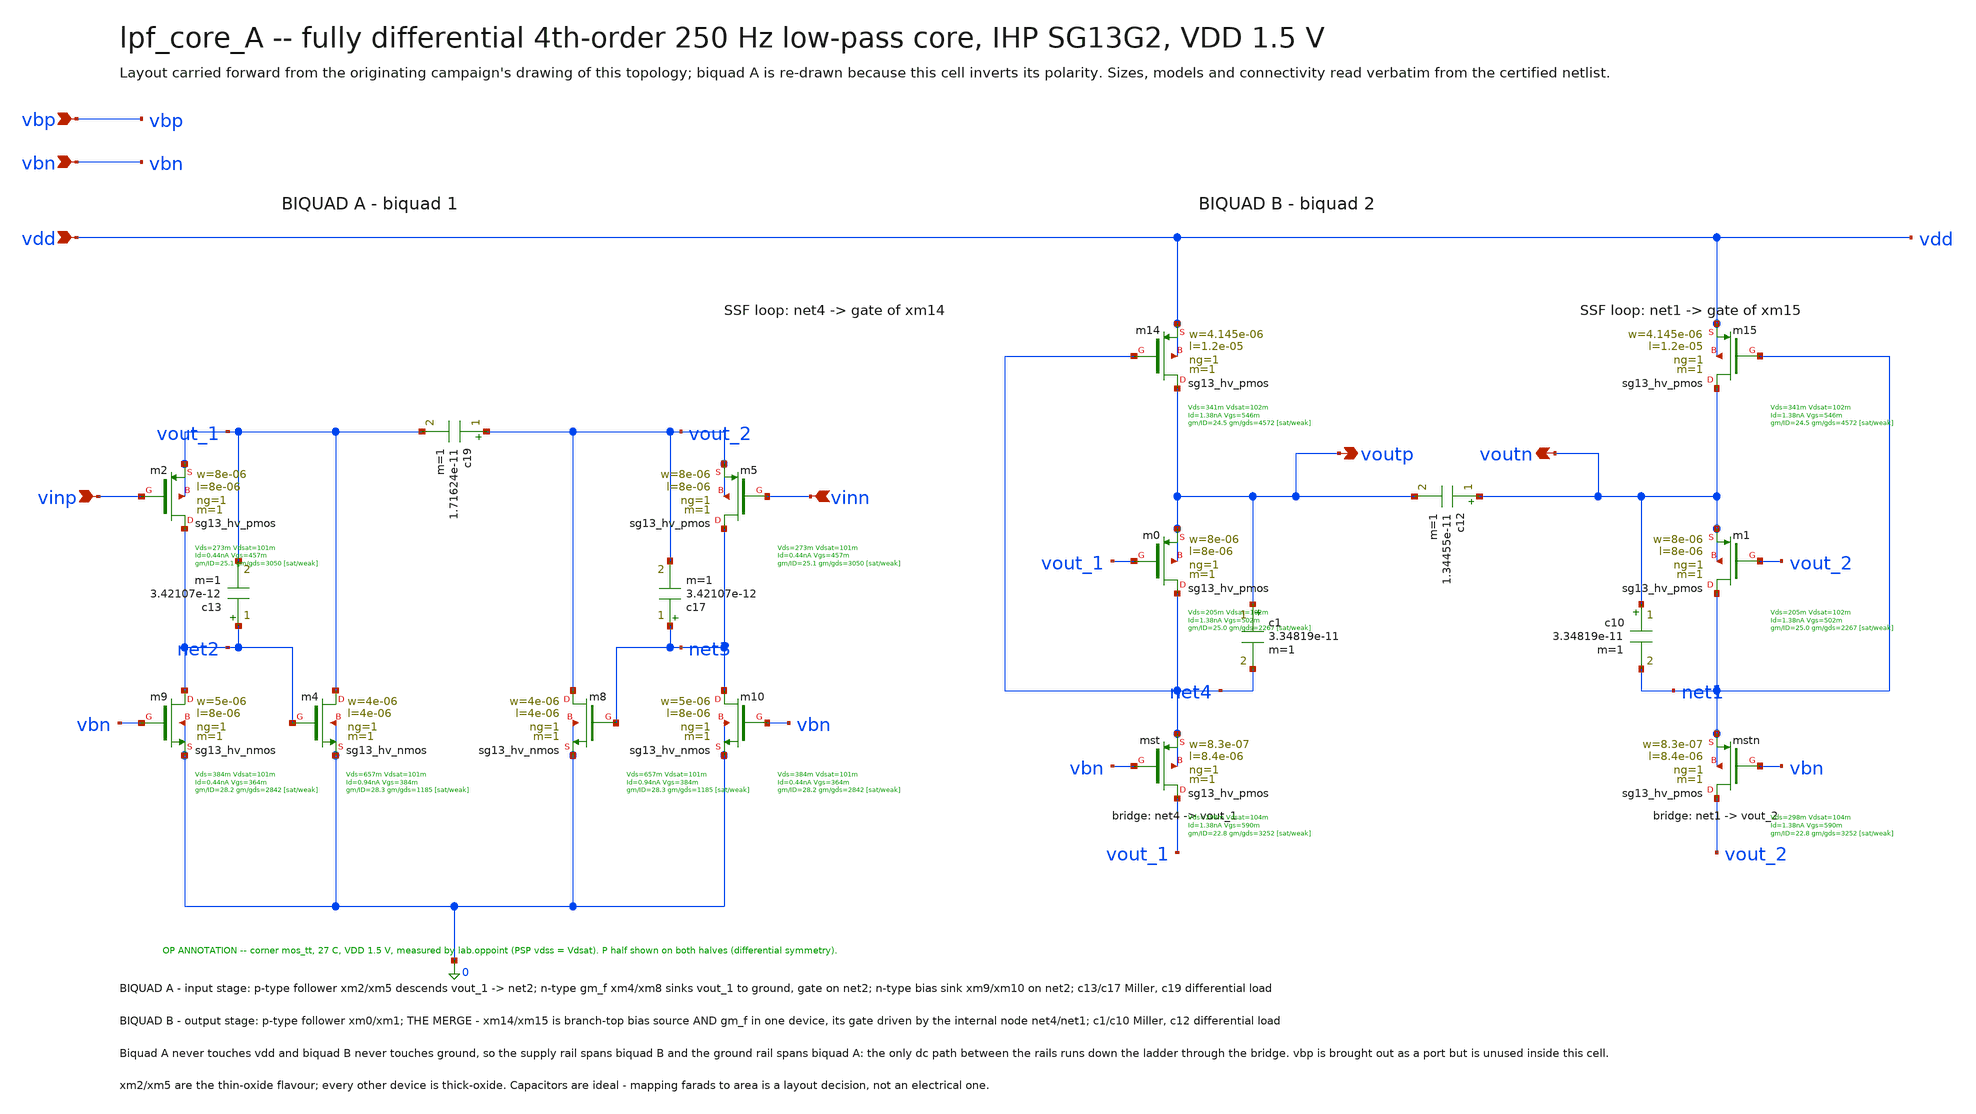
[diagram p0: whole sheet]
** sch_path: signoff/A-minarea/lpf_core_A.sch
**.subckt lpf_core_A vinp vinn voutp voutn vdd vbn vbp
*.ipin vinp
*.ipin vinn
*.opin voutp
*.opin voutn
*.ipin vdd
*.ipin vbn
*.ipin vbp
Xm2 net2 vinp vout_1 vout_1 sg13_hv_pmos w=8e-06 l=8e-06 ng=1 m=1 mm_ok=1
Xm5 net3 vinn vout_2 vout_2 sg13_hv_pmos w=8e-06 l=8e-06 ng=1 m=1 mm_ok=1
Xm4 vout_1 net2 0 0 sg13_hv_nmos w=4e-06 l=4e-06 ng=1 m=1 mm_ok=1
Xm8 vout_2 net3 0 0 sg13_hv_nmos w=4e-06 l=4e-06 ng=1 m=1 mm_ok=1
Xm9 net2 vbn 0 0 sg13_hv_nmos w=5e-06 l=8e-06 ng=1 m=1 mm_ok=1
Xm10 net3 vbn 0 0 sg13_hv_nmos w=5e-06 l=8e-06 ng=1 m=1 mm_ok=1
Xmst vout_1 vbn net4 net4 sg13_hv_pmos w=8.3e-07 l=8.4e-06 ng=1 m=1 mm_ok=1
Xmstn vout_2 vbn net1 net1 sg13_hv_pmos w=8.3e-07 l=8.4e-06 ng=1 m=1 mm_ok=1
Xm0 net4 vout_1 voutp voutp sg13_hv_pmos w=8e-06 l=8e-06 ng=1 m=1 mm_ok=1
Xm1 net1 vout_2 voutn voutn sg13_hv_pmos w=8e-06 l=8e-06 ng=1 m=1 mm_ok=1
Xm14 voutp net4 vdd vdd sg13_hv_pmos w=4.145e-06 l=1.2e-05 ng=1 m=1 mm_ok=1
Xm15 voutn net1 vdd vdd sg13_hv_pmos w=4.145e-06 l=1.2e-05 ng=1 m=1 mm_ok=1
c13 net2 vout_1 3.42107e-12 m=1
c17 net3 vout_2 3.42107e-12 m=1
c19 vout_2 vout_1 1.71624e-11 m=1
c1 voutp net4 3.34819e-11 m=1
c10 voutn net1 3.34819e-11 m=1
c12 voutn voutp 1.34455e-11 m=1
**.ends
.end
